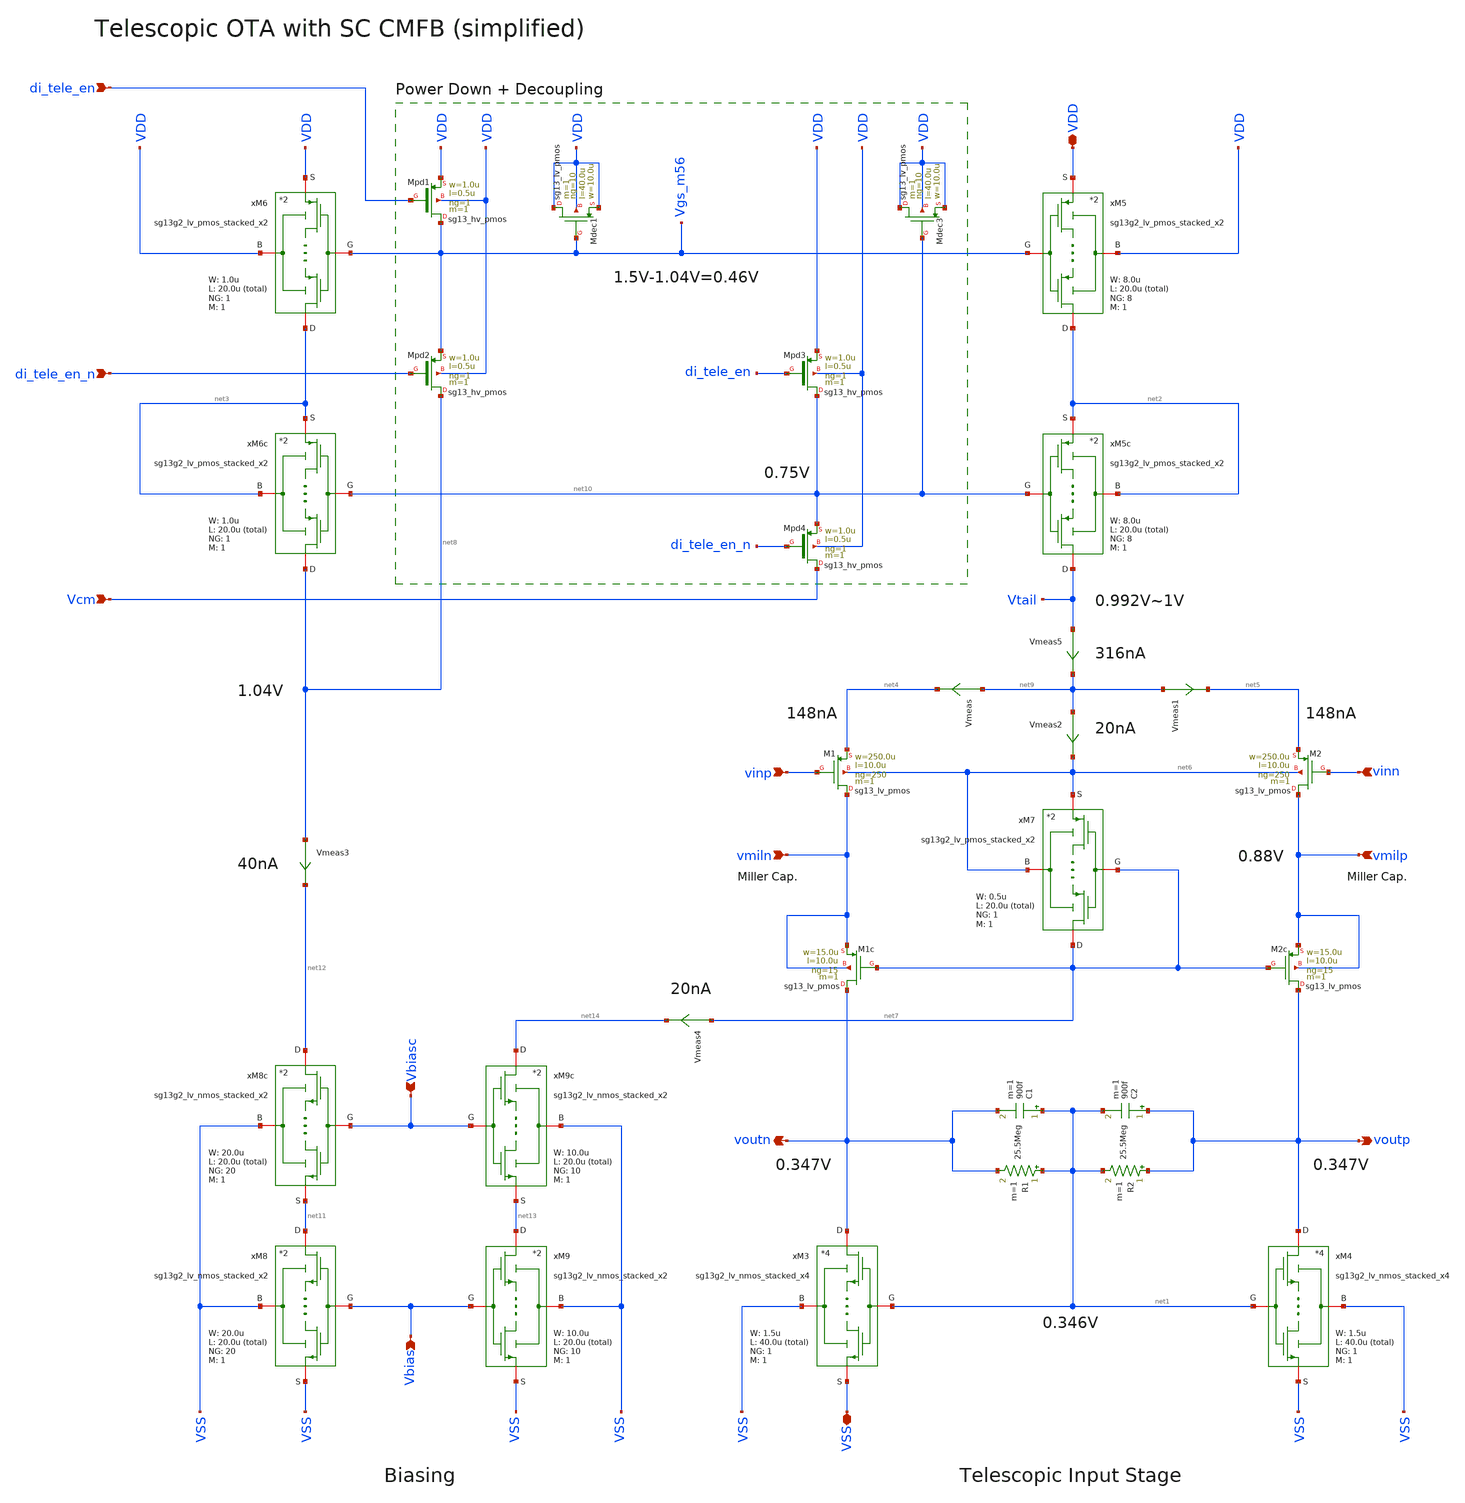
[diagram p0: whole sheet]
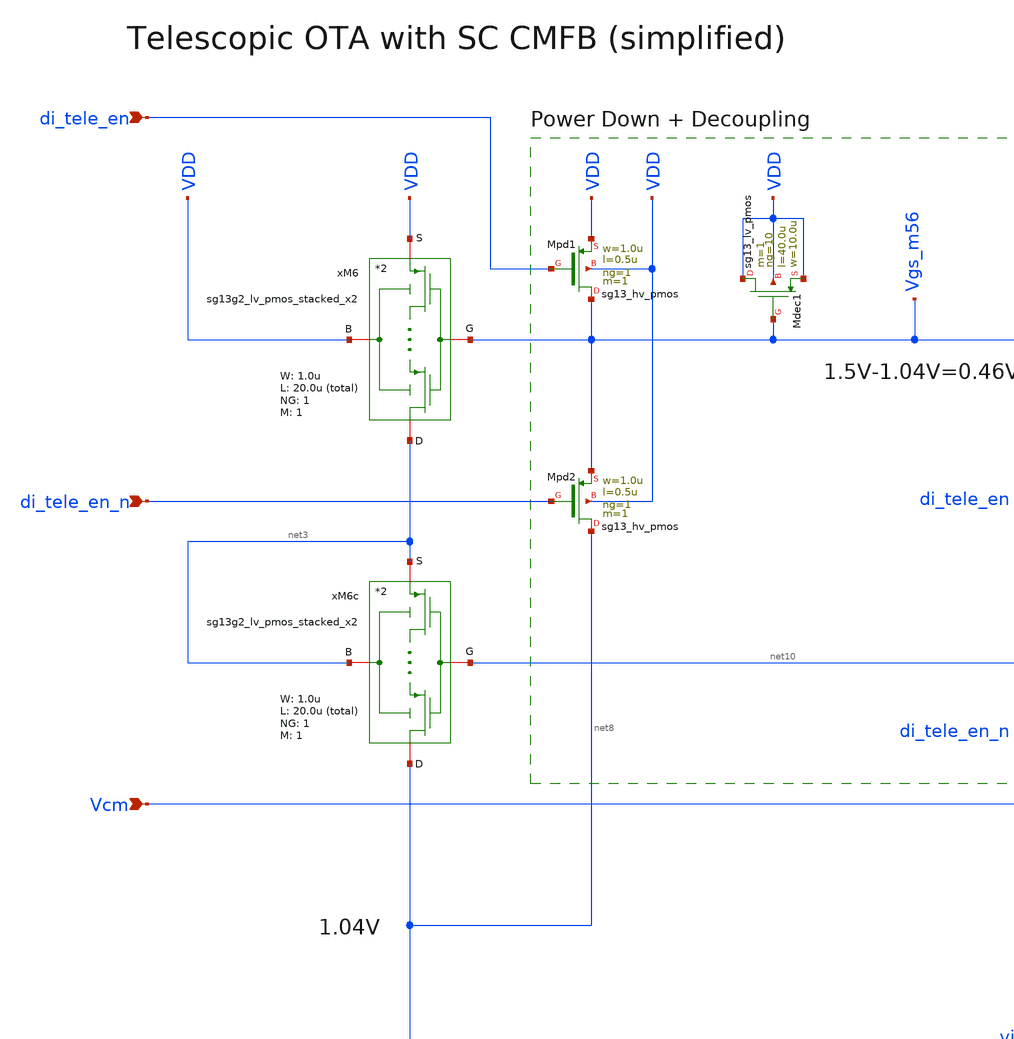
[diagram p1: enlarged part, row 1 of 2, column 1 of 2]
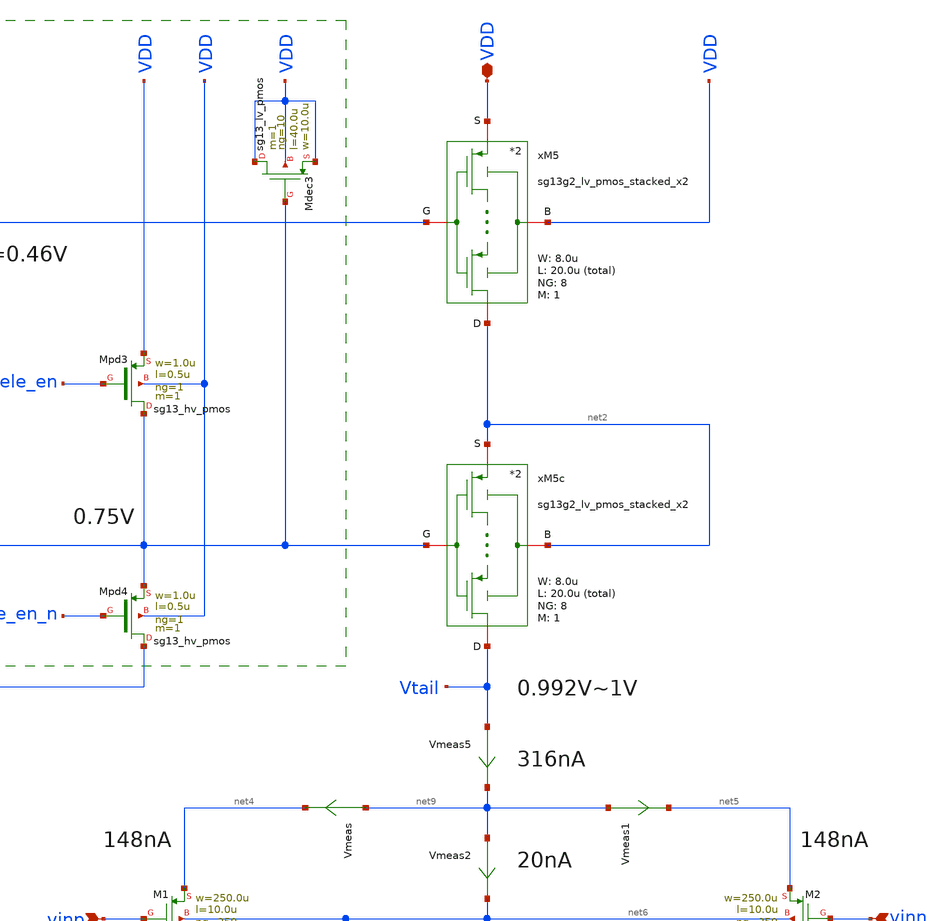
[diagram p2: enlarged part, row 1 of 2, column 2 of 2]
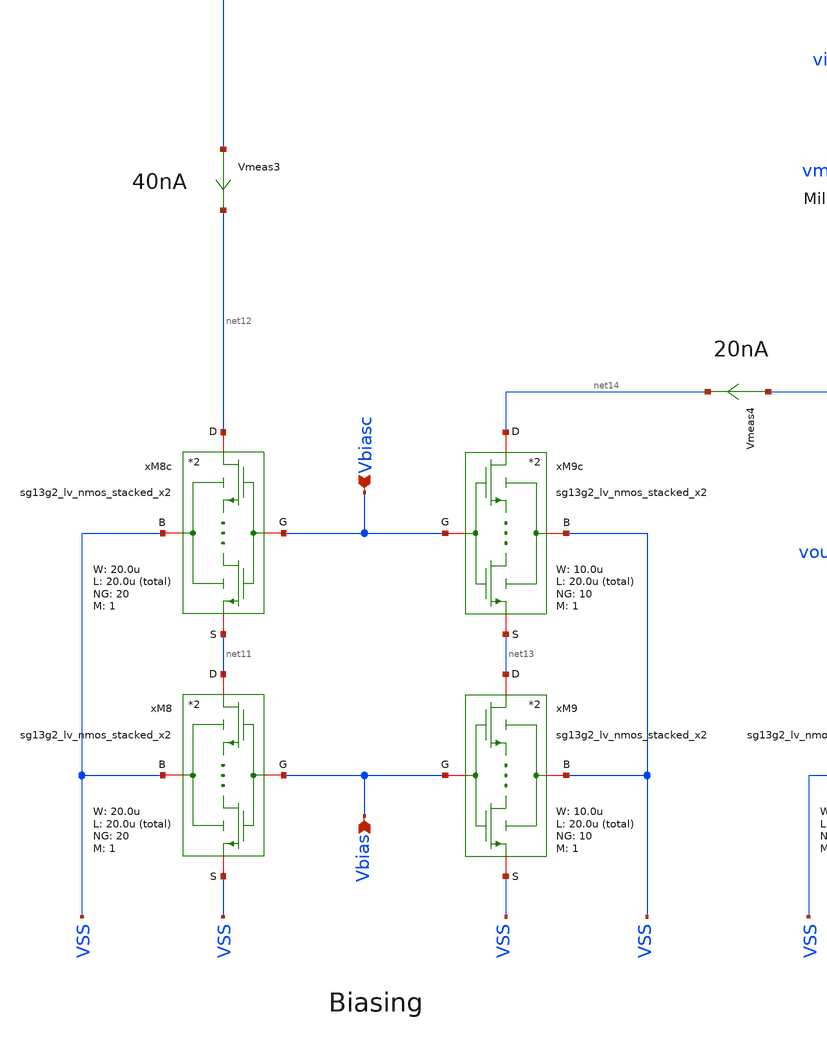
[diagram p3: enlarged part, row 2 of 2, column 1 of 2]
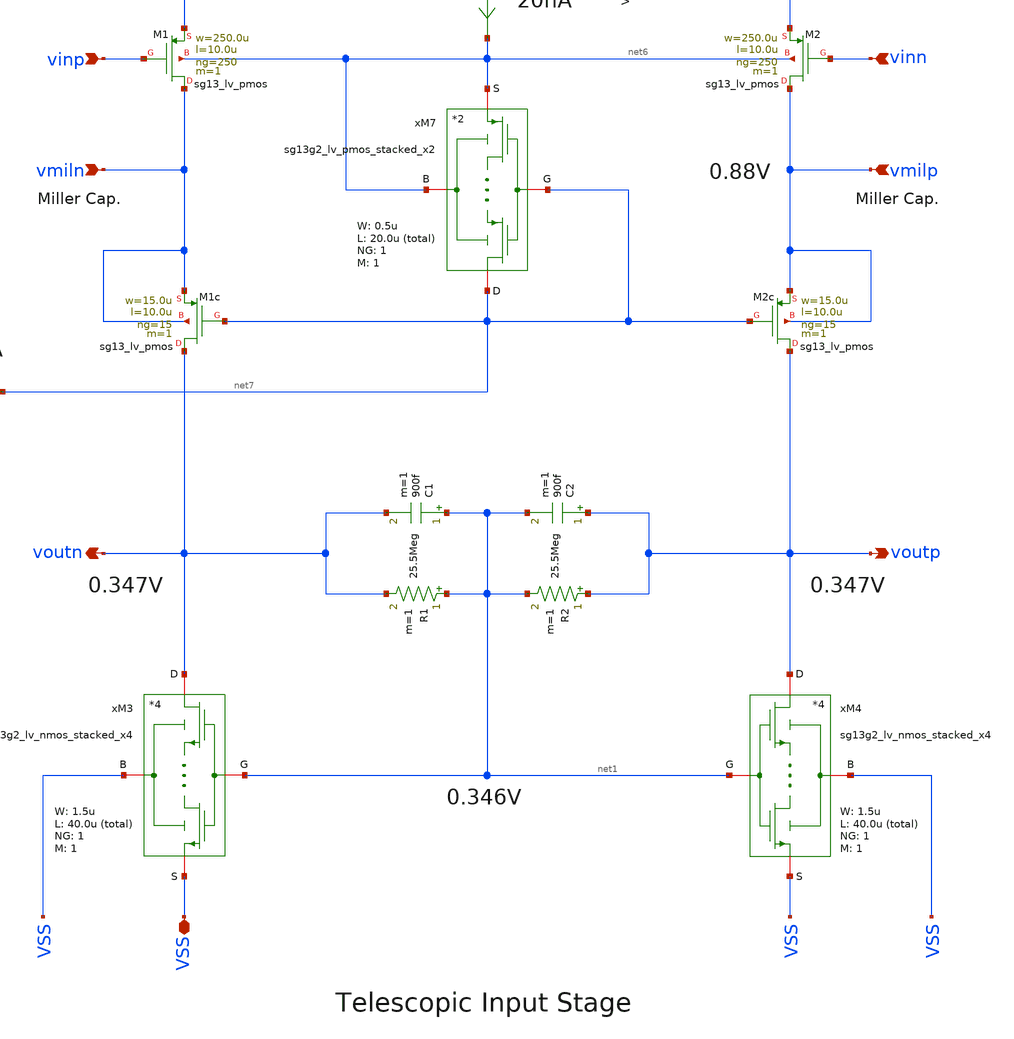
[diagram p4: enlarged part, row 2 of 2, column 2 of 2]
** sch_path: SG13G2_ATBS-ADC-main/xschem/bio_amplifier/amplifier_core/telescopic_ota/telescopic_ota_simplified.sch
**.subckt telescopic_ota_simplified vinp vinn voutp voutn VDD VSS Vcm di_tele_en di_tele_en_n vmilp
*+ vmiln Vbias Vbiasc
*.ipin vinp
*.ipin vinn
*.opin voutp
*.opin voutn
*.iopin VDD
*.iopin VSS
*.ipin Vcm
*.ipin di_tele_en
*.ipin di_tele_en_n
*.ipin vmilp
*.ipin vmiln
*.ipin Vbias
*.ipin Vbiasc
R1 net1 voutn 25.5Meg m=1
C1 net1 voutn 900f m=1
C2 voutp net1 900f m=1
R2 voutp net1 25.5Meg m=1
xM6 net3 Vgs_m56 VDD VDD sg13g2_lv_pmos_stacked_x2 W_P=1.0u L_P=20.0u NG_P=1 M_P=1
xM5 net2 Vgs_m56 VDD VDD sg13g2_lv_pmos_stacked_x2 W_P=8.0u L_P=20.0u NG_P=8 M_P=1
xM5c Vtail net10 net2 net2 sg13g2_lv_pmos_stacked_x2 W_P=8.0u L_P=20.0u NG_P=8 M_P=1
xM7 net7 net7 net6 net6 sg13g2_lv_pmos_stacked_x2 W_P=0.5u L_P=20.0u NG_P=1 M_P=1
XM1 vmiln vinp net4 net6 sg13_lv_pmos w=250.0u l=10.0u ng=250 m=1 mm_ok=1
XM1c voutn net7 vmiln vmiln sg13_lv_pmos w=15.0u l=10.0u ng=15 m=1 mm_ok=1
XM2c voutp net7 vmilp vmilp sg13_lv_pmos w=15.0u l=10.0u ng=15 m=1 mm_ok=1
XM2 vmilp vinn net5 net6 sg13_lv_pmos w=250.0u l=10.0u ng=250 m=1 mm_ok=1
xM3 voutn net1 VSS VSS sg13g2_lv_nmos_stacked_x4 W_N=1.5u L_N=40.0u NG_N=1 M_N=1
xM4 voutp net1 VSS VSS sg13g2_lv_nmos_stacked_x4 W_N=1.5u L_N=40.0u NG_N=1 M_N=1
Vmeas net9 net4 0
.save i(vmeas)
Vmeas1 net9 net5 0
.save i(vmeas1)
Vmeas2 net9 net6 0
.save i(vmeas2)
xM6c net8 net10 net3 net3 sg13g2_lv_pmos_stacked_x2 W_P=1.0u L_P=20.0u NG_P=1 M_P=1
XMpd4 Vcm di_tele_en_n net10 VDD sg13_hv_pmos w=1.0u l=0.5u ng=1 m=1 mm_ok=1
XMdec1 VDD Vgs_m56 VDD VDD sg13_lv_pmos w=10.0u l=40.0u ng=10 m=1 mm_ok=1
XMpd3 net10 di_tele_en VDD VDD sg13_hv_pmos w=1.0u l=0.5u ng=1 m=1 mm_ok=1
XMpd2 net8 di_tele_en_n Vgs_m56 VDD sg13_hv_pmos w=1.0u l=0.5u ng=1 m=1 mm_ok=1
XMpd1 Vgs_m56 di_tele_en VDD VDD sg13_hv_pmos w=1.0u l=0.5u ng=1 m=1 mm_ok=1
XMdec3 VDD net10 VDD VDD sg13_lv_pmos w=10.0u l=40.0u ng=10 m=1 mm_ok=1
Vmeas3 net8 net12 0
.save i(vmeas3)
Vmeas4 net7 net14 0
.save i(vmeas4)
xM8c net12 Vbiasc VSS net11 sg13g2_lv_nmos_stacked_x2 W_N=20.0u L_N=20.0u NG_N=20 M_N=1
xM8 net11 Vbias VSS VSS sg13g2_lv_nmos_stacked_x2 W_N=20.0u L_N=20.0u NG_N=20 M_N=1
xM9c net14 Vbiasc VSS net13 sg13g2_lv_nmos_stacked_x2 W_N=10.0u L_N=20.0u NG_N=10 M_N=1
xM9 net13 Vbias VSS VSS sg13g2_lv_nmos_stacked_x2 W_N=10.0u L_N=20.0u NG_N=10 M_N=1
Vmeas5 Vtail net9 0
.save i(vmeas5)
**.ends

* expanding   symbol:  stacked_transistors/sg13g2_lv_pmos_stacked/sg13g2_lv_pmos_stacked_x2.sym # of
*+ pins=4
** sym_path: SG13G2_ATBS-ADC-main/xschem/stacked_transistors/sg13g2_lv_pmos_stacked/sg13g2_lv_pmos_stacked_x2.sym
** sch_path: SG13G2_ATBS-ADC-main/xschem/stacked_transistors/sg13g2_lv_pmos_stacked/sg13g2_lv_pmos_stacked_x2.sch
.subckt sg13g2_lv_pmos_stacked_x2 D G B S  W_P=1.0u L_P=0.45u NG_P=1 M_P=1
*.iopin D
*.iopin S
*.iopin G
*.iopin B
XM1 net1 G S B sg13_lv_pmos w=W_P l=L_P/2 ng=NG_P m=M_P mm_ok=1
XM2 D G net1 B sg13_lv_pmos w=W_P l=L_P/2 ng=NG_P m=M_P mm_ok=1
.ends


* expanding   symbol:  stacked_transistors/sg13g2_lv_nmos_stacked/sg13g2_lv_nmos_stacked_x4.sym # of
*+ pins=4
** sym_path: SG13G2_ATBS-ADC-main/xschem/stacked_transistors/sg13g2_lv_nmos_stacked/sg13g2_lv_nmos_stacked_x4.sym
** sch_path: SG13G2_ATBS-ADC-main/xschem/stacked_transistors/sg13g2_lv_nmos_stacked/sg13g2_lv_nmos_stacked_x4.sch
.subckt sg13g2_lv_nmos_stacked_x4 D G B S  W_N=1.0u L_N=0.45u NG_N=1 M_N=1
*.iopin D
*.iopin S
*.iopin G
*.iopin B
XM1 net1 G S B sg13_lv_nmos w=W_N l=L_N/4 ng=NG_N m=M_N mm_ok=1
XM2 net3 G net1 B sg13_lv_nmos w=W_N l=L_N/4 ng=NG_N m=M_N mm_ok=1
XM3 net2 G net3 B sg13_lv_nmos w=W_N l=L_N/4 ng=NG_N m=M_N mm_ok=1
XM4 D G net2 B sg13_lv_nmos w=W_N l=L_N/4 ng=NG_N m=M_N mm_ok=1
.ends


* expanding   symbol:  stacked_transistors/sg13g2_lv_nmos_stacked/sg13g2_lv_nmos_stacked_x2.sym # of
*+ pins=4
** sym_path: SG13G2_ATBS-ADC-main/xschem/stacked_transistors/sg13g2_lv_nmos_stacked/sg13g2_lv_nmos_stacked_x2.sym
** sch_path: SG13G2_ATBS-ADC-main/xschem/stacked_transistors/sg13g2_lv_nmos_stacked/sg13g2_lv_nmos_stacked_x2.sch
.subckt sg13g2_lv_nmos_stacked_x2 D G B S  W_N=1.0u L_N=0.45u NG_N=1 M_N=1
*.iopin D
*.iopin S
*.iopin G
*.iopin B
XM1 net1 G S B sg13_lv_nmos w=W_N l=L_N/2 ng=NG_N m=M_N mm_ok=1
XM2 D G net1 B sg13_lv_nmos w=W_N l=L_N/2 ng=NG_N m=M_N mm_ok=1
.ends

.end
